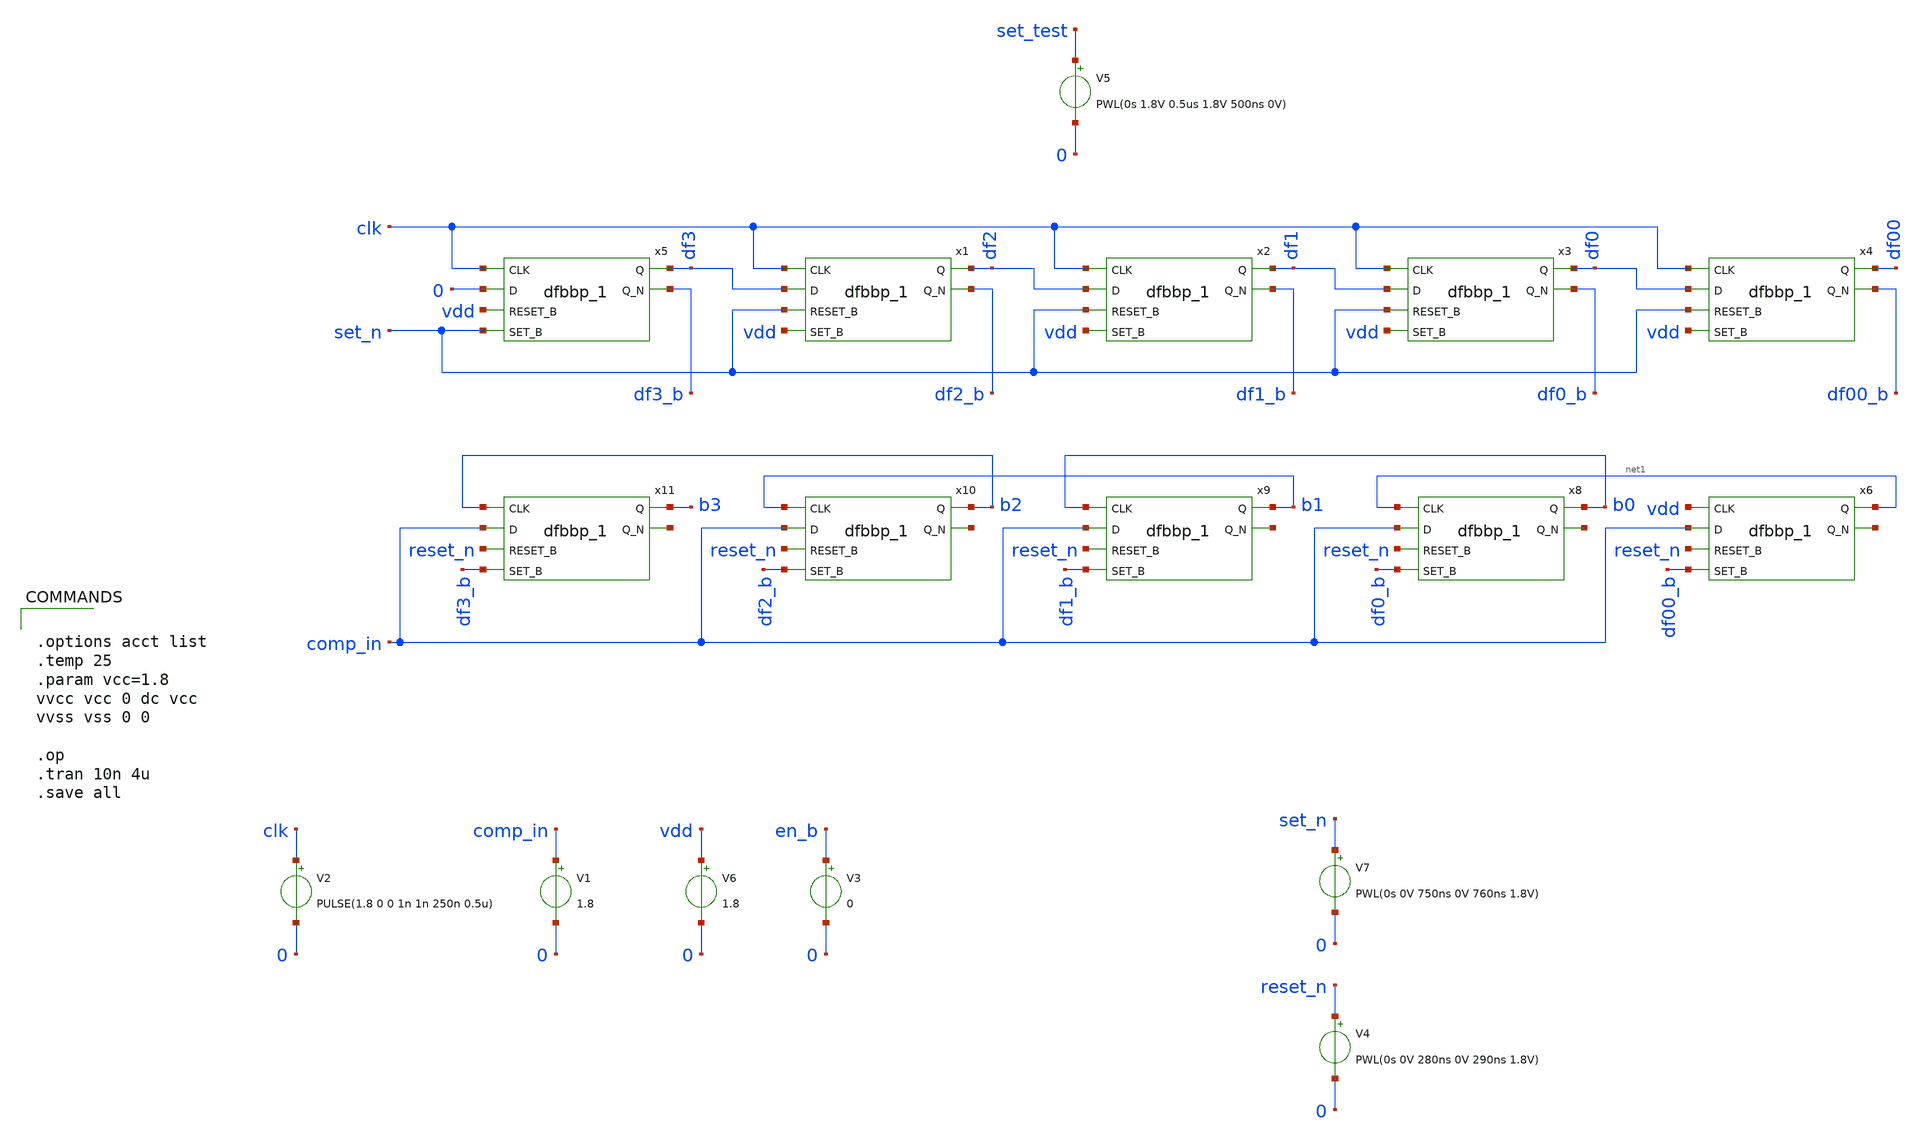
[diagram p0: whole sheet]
** sch_path: xschem/sar_logic/sar_logic_tb.sch
.lib $::SKYWATER_MODELS/sky130.lib.spice tt
.include $::SKYWATER_STDCELLS/sky130_fd_sc_hd.spice

**.subckt sar_logic_tb
V2 clk 0 PULSE(1.8 0 0 1n 1n 250n 0.5u)
V1 comp_in 0 1.8
V3 en_b 0 0
x5 clk 0 vdd set_n vss vss vcc vcc df3 df3_b sky130_fd_sc_hd__dfbbp_1
x1 clk df3 set_n vdd vss vss vcc vcc df2 df2_b sky130_fd_sc_hd__dfbbp_1
V4 reset_n 0 PWL(0s 0V 280ns 0V 290ns 1.8V)
V5 set_test 0 PWL(0s 1.8V 0.5us 1.8V 500ns 0V)
V6 vdd 0 1.8
x2 clk df2 set_n vdd vss vss vcc vcc df1 df1_b sky130_fd_sc_hd__dfbbp_1
x3 clk df1 set_n vdd vss vss vcc vcc df0 df0_b sky130_fd_sc_hd__dfbbp_1
x4 clk df0 set_n vdd vss vss vcc vcc df00 df00_b sky130_fd_sc_hd__dfbbp_1
x6 vdd comp_in reset_n df00_b vss vss vcc vcc net1 net2 sky130_fd_sc_hd__dfbbp_1
x8 net1 comp_in reset_n df0_b vss vss vcc vcc b0 net3 sky130_fd_sc_hd__dfbbp_1
x9 b0 comp_in reset_n df1_b vss vss vcc vcc b1 net4 sky130_fd_sc_hd__dfbbp_1
x10 b1 comp_in reset_n df2_b vss vss vcc vcc b2 net5 sky130_fd_sc_hd__dfbbp_1
x11 b2 comp_in reset_n df3_b vss vss vcc vcc b3 net6 sky130_fd_sc_hd__dfbbp_1
V7 set_n 0 PWL(0s 0V 750ns 0V 760ns 1.8V)
**** begin user architecture code


.options acct list
.temp 25
.param vcc=1.8
vvcc vcc 0 dc vcc
vvss vss 0 0

.op
.tran 10n 4u
.save all


**** end user architecture code
**.ends
.end
